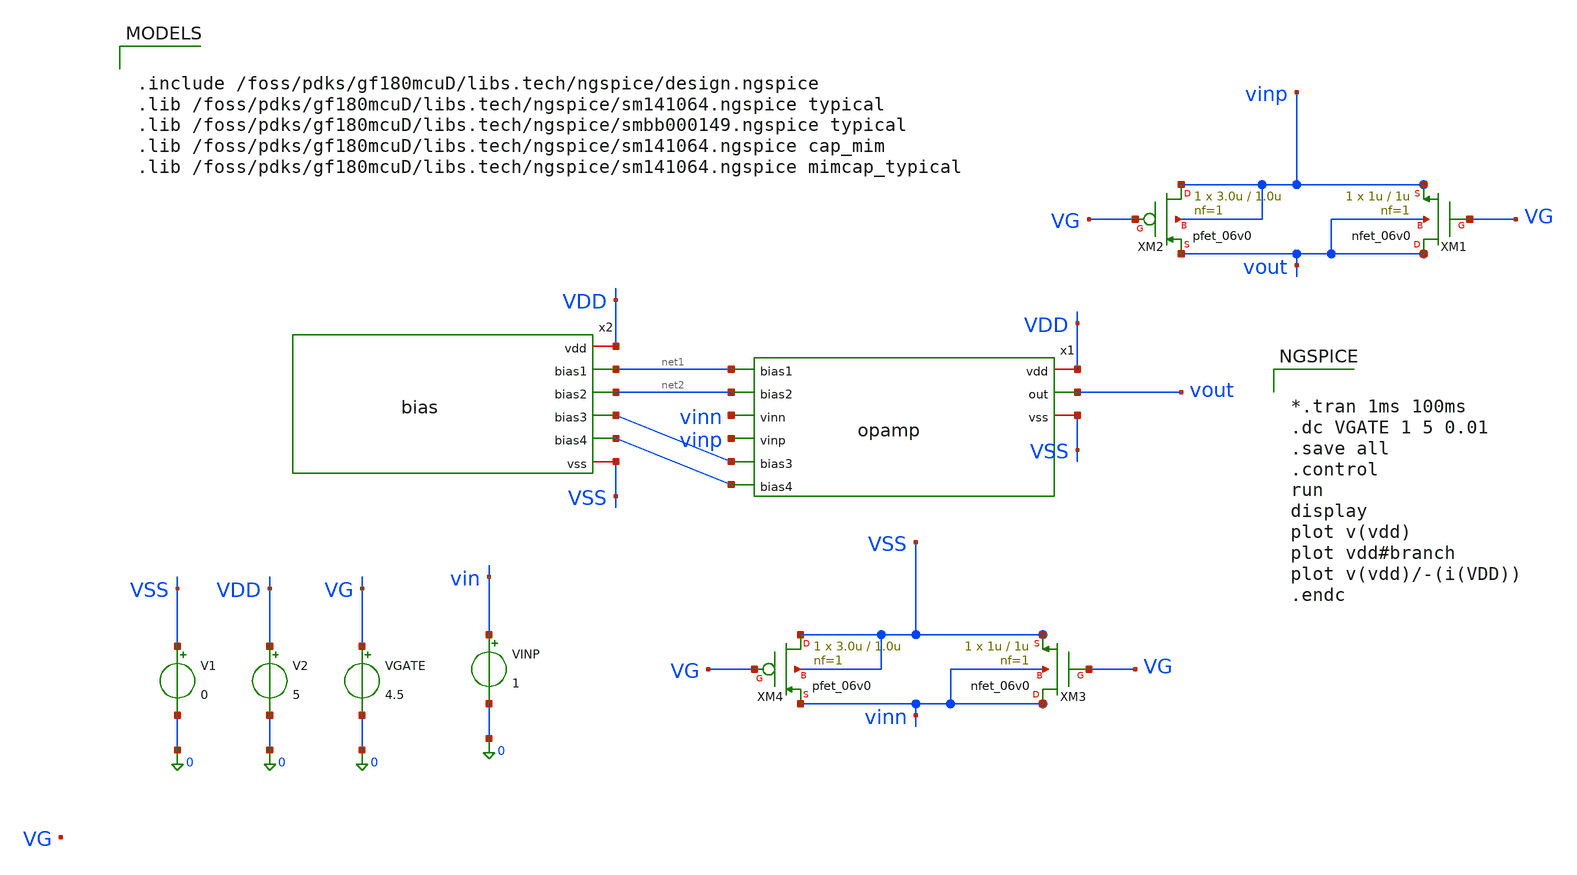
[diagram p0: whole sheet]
** sch_path: activities/opamp3An/untitled.sch
**.subckt untitled
x1 VDD net1 net2 vinn vout vinp net4 net3 VSS opamp
x2 VDD net1 net2 net4 net3 VSS bias
V1 VSS 0 0
V2 VDD 0 5
VGATE VG 0 4.5
VINP vin 0 1
XM1 vout VG vinp vout nfet_06v0 L=1u W=1u nf=1 ad='int((nf+1)/2) * W/nf * 0.18u' as='int((nf+2)/2) * W/nf * 0.18u'
+ pd='2*int((nf+1)/2) * (W/nf + 0.18u)' ps='2*int((nf+2)/2) * (W/nf + 0.18u)' nrd='0.18u / W' nrs='0.18u / W'
+ sa=0 sb=0 sd=0 m=1
XM2 vinp VG vout vinp pfet_06v0 L=1.0u W=3.0u nf=1 ad='int((nf+1)/2) * W/nf * 0.18u' as='int((nf+2)/2) * W/nf * 0.18u'
+ pd='2*int((nf+1)/2) * (W/nf + 0.18u)' ps='2*int((nf+2)/2) * (W/nf + 0.18u)' nrd='0.18u / W' nrs='0.18u / W'
+ sa=0 sb=0 sd=0 m=1
XM3 vinn VG VSS vinn nfet_06v0 L=1u W=1u nf=1 ad='int((nf+1)/2) * W/nf * 0.18u' as='int((nf+2)/2) * W/nf * 0.18u'
+ pd='2*int((nf+1)/2) * (W/nf + 0.18u)' ps='2*int((nf+2)/2) * (W/nf + 0.18u)' nrd='0.18u / W' nrs='0.18u / W'
+ sa=0 sb=0 sd=0 m=1
XM4 VSS VG vinn VSS pfet_06v0 L=1.0u W=3.0u nf=1 ad='int((nf+1)/2) * W/nf * 0.18u' as='int((nf+2)/2) * W/nf * 0.18u'
+ pd='2*int((nf+1)/2) * (W/nf + 0.18u)' ps='2*int((nf+2)/2) * (W/nf + 0.18u)' nrd='0.18u / W' nrs='0.18u / W'
+ sa=0 sb=0 sd=0 m=1
**** begin user architecture code


.include /foss/pdks/gf180mcuD/libs.tech/ngspice/design.ngspice
.lib /foss/pdks/gf180mcuD/libs.tech/ngspice/sm141064.ngspice typical
.lib /foss/pdks/gf180mcuD/libs.tech/ngspice/smbb000149.ngspice typical
.lib /foss/pdks/gf180mcuD/libs.tech/ngspice/sm141064.ngspice cap_mim
.lib /foss/pdks/gf180mcuD/libs.tech/ngspice/sm141064.ngspice mimcap_typical




*.tran 1ms 100ms
.dc VGATE 1 5 0.01
.save all
.control
run
display
plot v(vdd)
plot vdd#branch
plot v(vdd)/-(i(VDD))
.endc


**** end user architecture code
**.ends
.end
